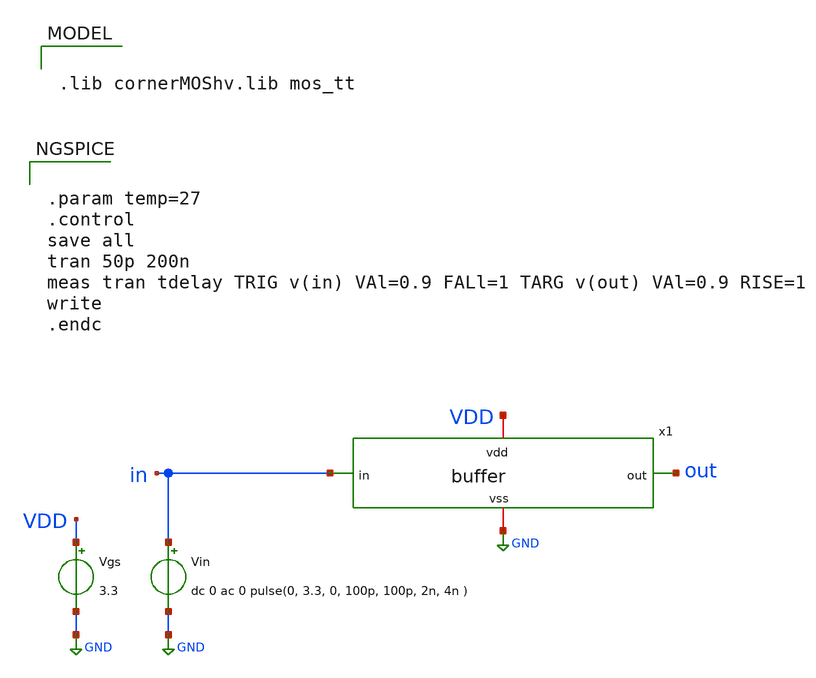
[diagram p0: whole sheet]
** sch_path: buffer/tb_buffer.sch
**.subckt tb_buffer
Vgs VDD GND 3.3
Vin in GND dc 0 ac 0 pulse(0, 3.3, 0, 100p, 100p, 2n, 4n )
x1 VDD in out GND buffer
**** begin user architecture code


.lib cornerMOShv.lib mos_tt




.param temp=27
.control
save all
tran 50p 200n
meas tran tdelay TRIG v(in) VAl=0.9 FALl=1 TARG v(out) VAl=0.9 RISE=1
write
.endc


**** end user architecture code
**.ends
.GLOBAL GND
.end
